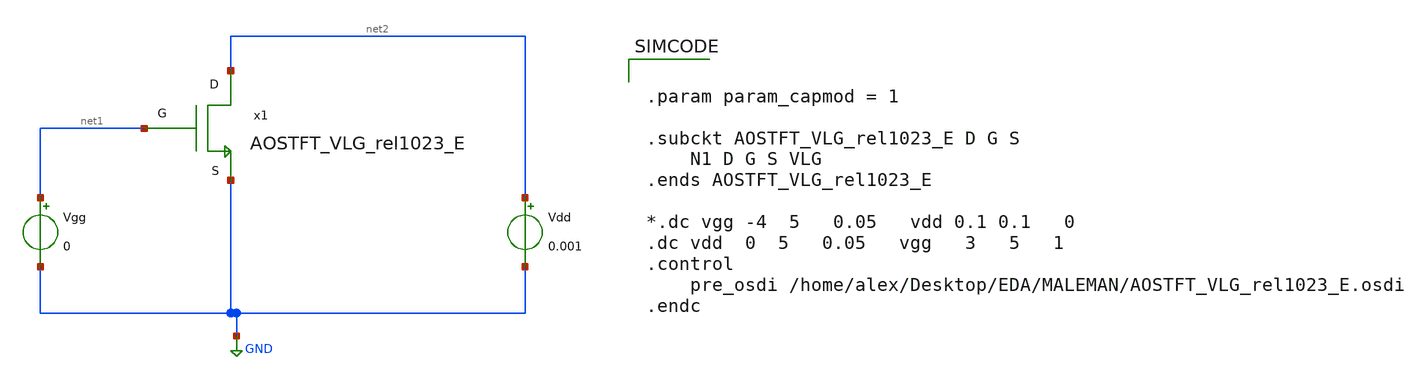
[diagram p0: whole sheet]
** sch_path: tb_AOSTFT_VLG_rel1023_E_tb.sch
**.subckt tb_AOSTFT_VLG_rel1023_E_tb
Vgg net1 GND 0
Vdd net2 GND 0.001
x1 net2 net1 GND AOSTFT_VLG_rel1023_E
**** begin user architecture code



.model VLG TFT TYPE =1				 TNOM		=27 L		=40e-6 W		=160e-6 TOX		=22e-9 TSI		=15e-9 TPAS		=400e-9
+ LOVDS		=5e-6 LOVTDS		=5e-6 EPS		=9 EPSI		=7 EPSPAS		=3.9 MU1		=8.98 VT0		=-2.27 GAMMA		=0.259 RS		=75 RD
+         	=75 ALPHAS		=0.727 M		=1.63 LAMBDA		=-0.0569 DELTA		=0 MUB1		=3.81 GAMMAB		=0.76 VFB		=-2.89 S		=0.237
+ V1A		=-1.793 V1		=-0.47 Q1		=33.7 V2		=1.11 Q2		=0.66 I0		=5E-13 VDSlin		=0.1 V3		=0 Q3		=0 ALPHASS	=0
+ CGGDEP		=4.1e-12 CGGACU		=19.6e-12 MM		=0.0 a		=0.00 DD		=0.0 VAC		=0. capmod 	=param_capmod




.param param_capmod = 1

.subckt AOSTFT_VLG_rel1023_E D G S
	N1 D G S VLG
.ends AOSTFT_VLG_rel1023_E

*.dc vgg -4  5   0.05   vdd 0.1 0.1   0
.dc vdd  0  5   0.05   vgg   3   5   1
.control
	pre_osdi /home/alex/Desktop/EDA/MALEMAN/AOSTFT_VLG_rel1023_E.osdi
.endc


**** end user architecture code
**.ends
.GLOBAL GND
.end
